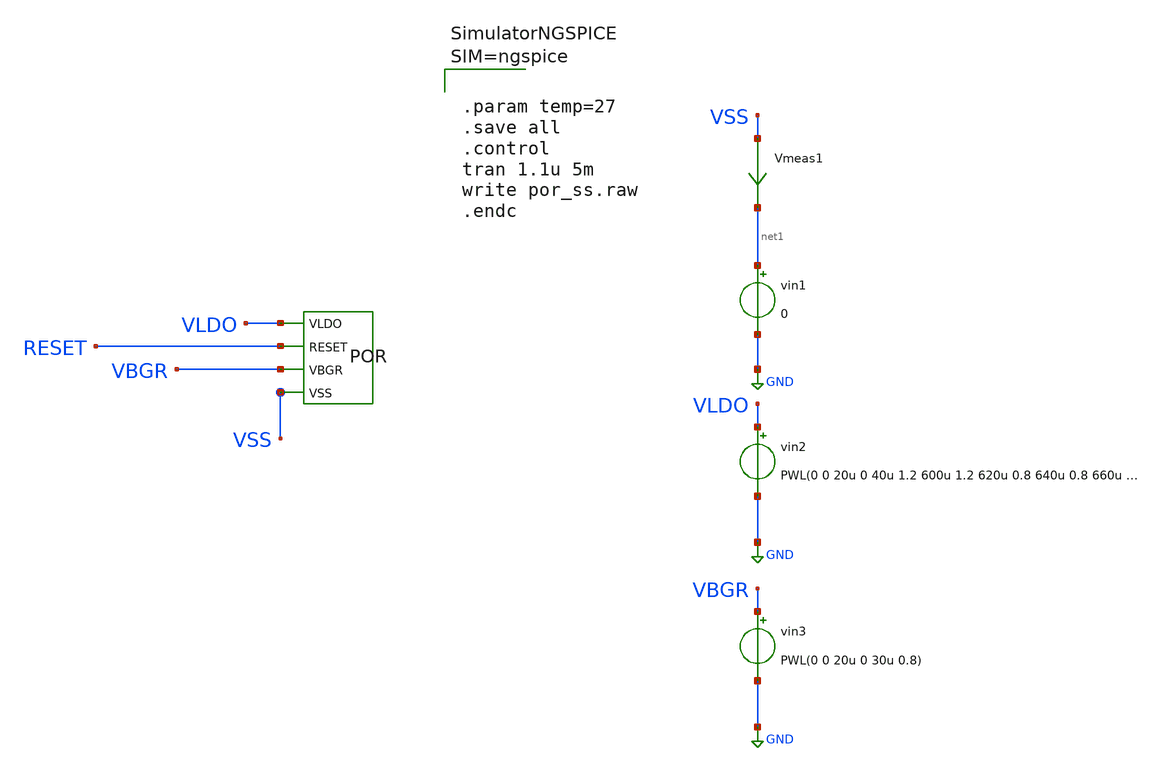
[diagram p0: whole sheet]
** sch_path: dependencies/POR/POR-main/testbenches/corners/xschem/por_post_layout_sim_ss.sch
**.subckt por_post_layout_sim_ss
X1 VLDO RESET VBGR VSS POR
vin1 net1 GND 0
Vmeas1 VSS net1 0
.save i(vmeas1)
vin2 VLDO GND PWL(0 0 20u 0 40u 1.2 600u 1.2 620u 0.8 640u 0.8 660u 1.2 760u 1.2 780u 0)
vin3 VBGR GND PWL(0 0 20u 0 30u 0.8)
**** begin user architecture code



.include /foss/designs/simulations/POR/output/POR__POR/magic_RC/POR.pex.spice
.lib cornerMOSlv.lib mos_ss
.lib cornerMOShv.lib mos_ss
.lib cornerHBT.lib hbt_typ
.lib cornerRES.lib res_typ
.lib cornerDIO.lib dio_tt
.lib cornerCAP.lib cap_typ






.param temp=27
.save all
.control
tran 1.1u 5m
write por_ss.raw
.endc



**** end user architecture code
**.ends
.GLOBAL GND
.end
